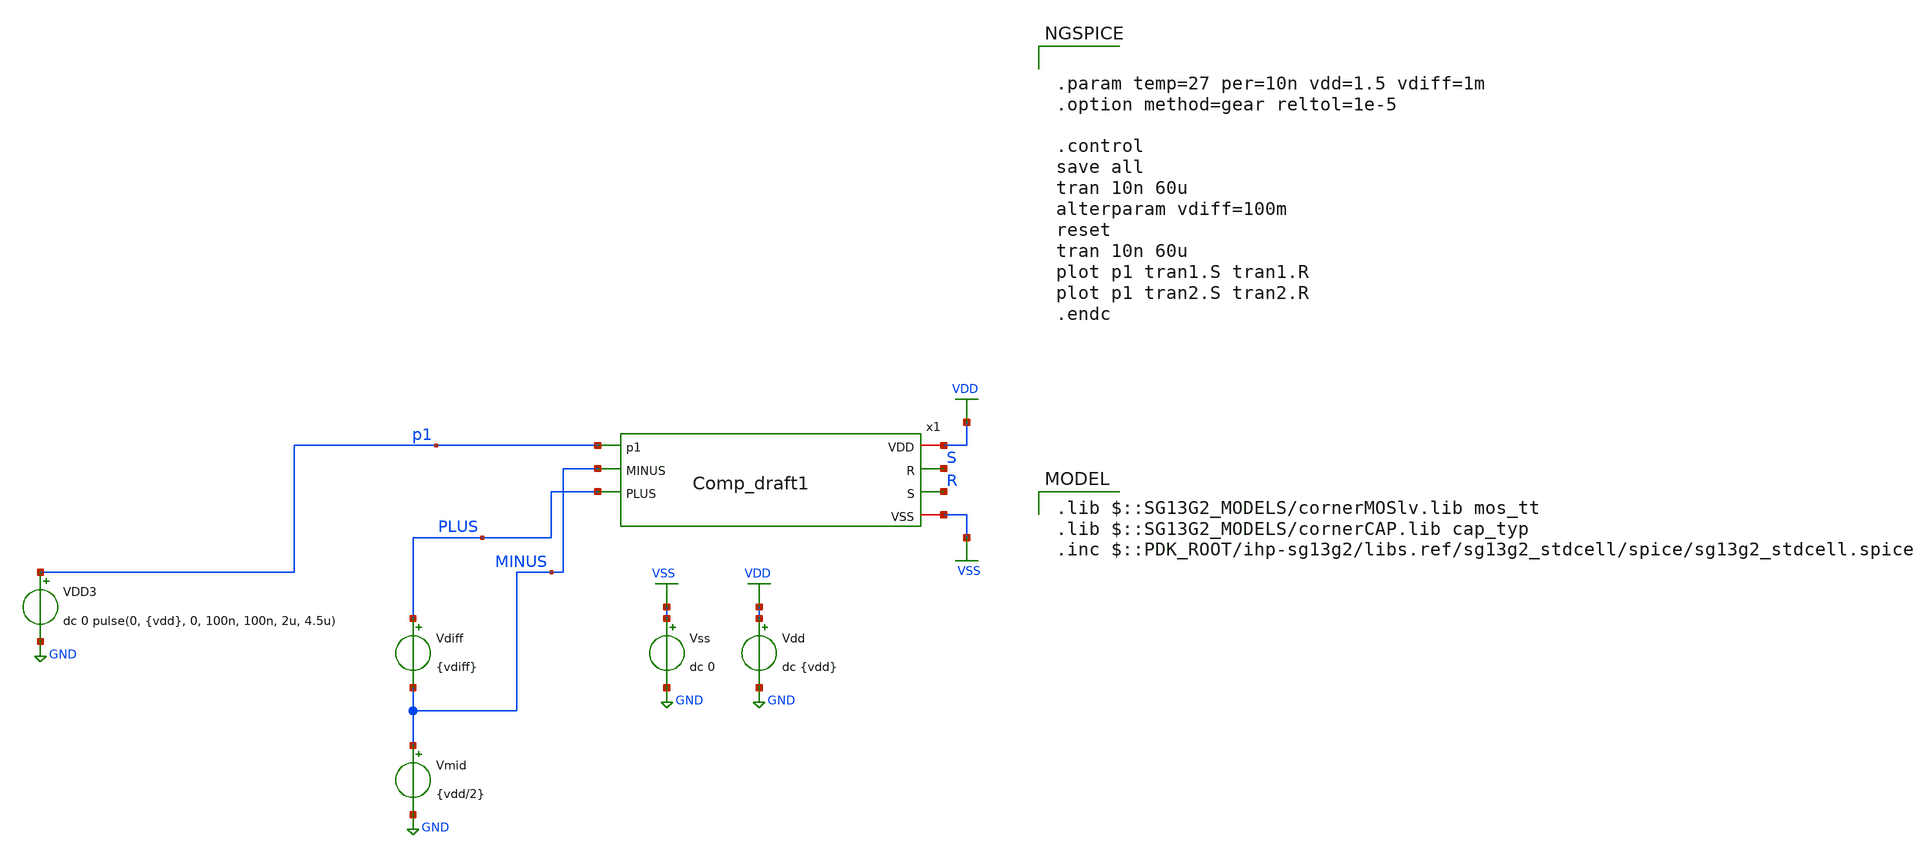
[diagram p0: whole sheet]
** sch_path: DSM/Schematics/Comparator_design_Sneha/COMPARATOR_FINAL/tb_Comp_draft1-2.sch
**.subckt tb_Comp_draft1-2
Vdd VDD GND dc {vdd}
Vss VSS GND dc 0
VDD3 p1 GND dc 0 pulse(0, {vdd}, 0, 100n, 100n, 2u, 4.5u)
Vdiff PLUS MINUS {vdiff}
Vmid MINUS GND {vdd/2}
x1 VDD p1 S R MINUS PLUS VSS Comp_draft1
**** begin user architecture code


.param temp=27 per=10n vdd=1.5 vdiff=1m
.option method=gear reltol=1e-5

.control
save all
tran 10n 60u
alterparam vdiff=100m
reset
tran 10n 60u
plot p1 tran1.S tran1.R
plot p1 tran2.S tran2.R
.endc


 .lib $::SG13G2_MODELS/cornerMOSlv.lib mos_tt
.lib $::SG13G2_MODELS/cornerCAP.lib cap_typ
.inc $::PDK_ROOT/ihp-sg13g2/libs.ref/sg13g2_stdcell/spice/sg13g2_stdcell.spice

**** end user architecture code
**.ends

* expanding   symbol:  Comp_draft1.sym # of pins=7
** sym_path: DSM/Schematics/Comparator_design_Sneha/COMPARATOR_FINAL/Comp_draft1.sym
** sch_path: DSM/Schematics/Comparator_design_Sneha/COMPARATOR_FINAL/Comp_draft1.sch
.subckt Comp_draft1 VDD p1 R S MINUS PLUS VSS
*.ipin PLUS
*.ipin MINUS
*.ipin p1
*.iopin VDD
*.iopin VSS
*.opin R
*.opin S
XMN5 S R net3 VSS sg13_lv_nmos w=1u l=0.18u ng=1 m=1 mm_ok=1
XMP7 net3 p1 VDD VDD sg13_lv_pmos w=0.5u l=0.18u ng=1 m=1 mm_ok=1
XMP8 S p1 VDD VDD sg13_lv_pmos w=0.5u l=0.18u ng=1 m=1 mm_ok=1
XMP9 S R VDD VDD sg13_lv_pmos w=2u l=0.18u ng=1 m=1 mm_ok=1
XMP10 R S VDD VDD sg13_lv_pmos w=2u l=0.18u ng=1 m=1 mm_ok=1
XMP11 R p1 VDD VDD sg13_lv_pmos w=0.5u l=0.18u ng=1 m=1 mm_ok=1
XMP12 net2 p1 VDD VDD sg13_lv_pmos w=0.5u l=0.15u ng=1 m=1 mm_ok=1
XMN6 R S net2 VSS sg13_lv_nmos w=1u l=0.18u ng=1 m=1 mm_ok=1
XMN7 net4 PLUS net1 VSS sg13_lv_nmos w=2u l=0.18u ng=1 m=1 mm_ok=1
XMN8 net2 MINUS net1 VSS sg13_lv_nmos w=2u l=0.18u ng=1 m=1 mm_ok=1
XM7 net1 p1 VSS VSS sg13_lv_nmos w=4u l=0.18u ng=1 m=1 mm_ok=1
.ends

.GLOBAL GND
.GLOBAL VDD
.GLOBAL VSS
.end
